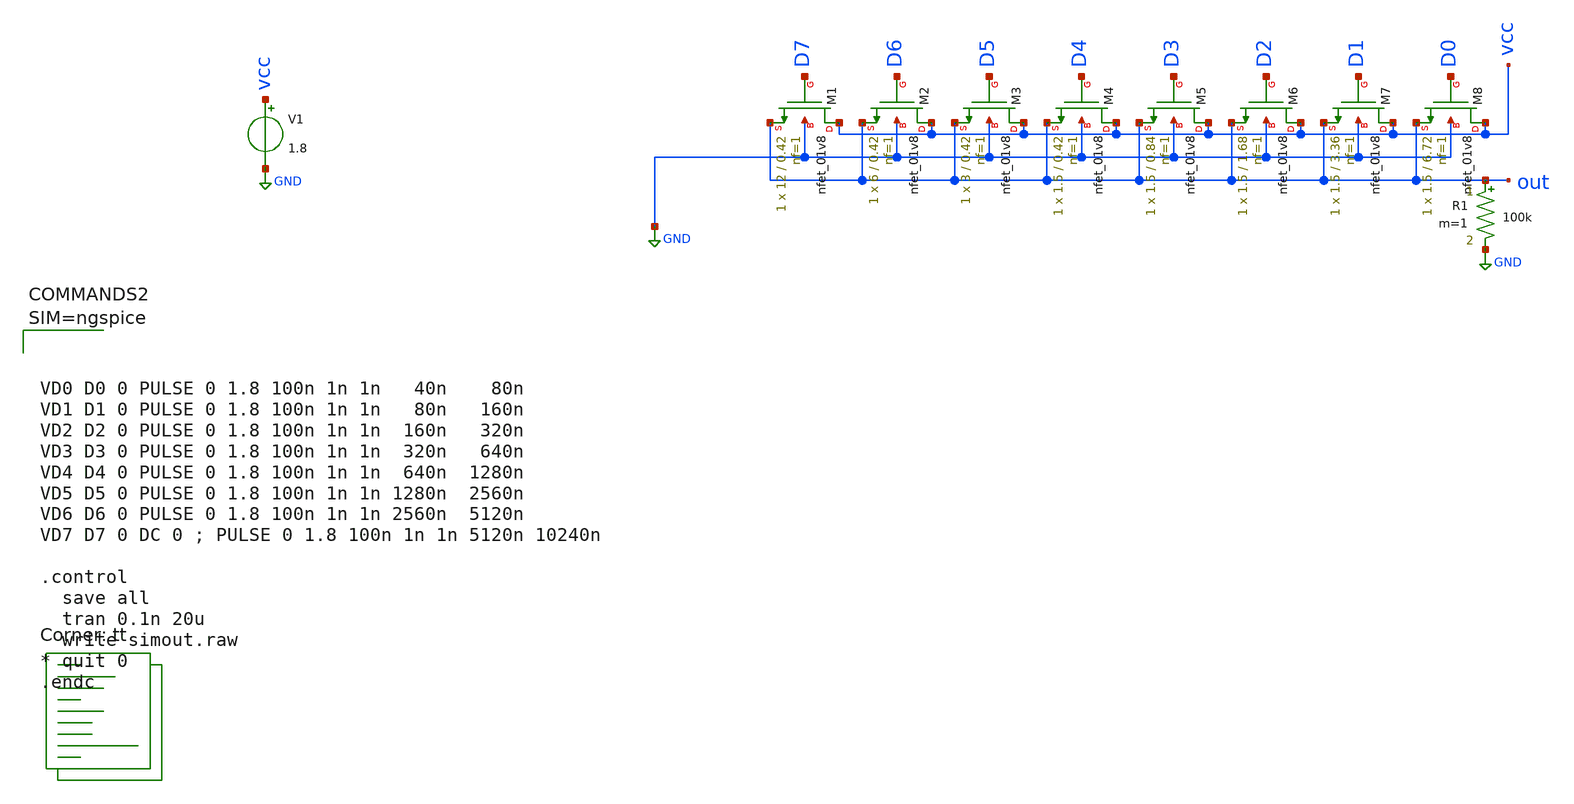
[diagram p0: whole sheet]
** sch_path: xschem/tbtemplate.sch
**.subckt tbtemplate
XM1 vcc D7 out GND sky130_fd_pr__nfet_01v8 L=0.42 W=12 nf=1 ad='int((nf+1)/2) * W/nf * 0.29' as='int((nf+2)/2) * W/nf * 0.29'
+ pd='2*int((nf+1)/2) * (W/nf + 0.29)' ps='2*int((nf+2)/2) * (W/nf + 0.29)' nrd='0.29 / W' nrs='0.29 / W'
+ sa=0 sb=0 sd=0 mult=1 m=1
V1 vcc GND 1.8
XM2 vcc D6 out GND sky130_fd_pr__nfet_01v8 L=0.42 W=6 nf=1 ad='int((nf+1)/2) * W/nf * 0.29' as='int((nf+2)/2) * W/nf * 0.29'
+ pd='2*int((nf+1)/2) * (W/nf + 0.29)' ps='2*int((nf+2)/2) * (W/nf + 0.29)' nrd='0.29 / W' nrs='0.29 / W'
+ sa=0 sb=0 sd=0 mult=1 m=1
XM3 vcc D5 out GND sky130_fd_pr__nfet_01v8 L=0.42 W=3 nf=1 ad='int((nf+1)/2) * W/nf * 0.29' as='int((nf+2)/2) * W/nf * 0.29'
+ pd='2*int((nf+1)/2) * (W/nf + 0.29)' ps='2*int((nf+2)/2) * (W/nf + 0.29)' nrd='0.29 / W' nrs='0.29 / W'
+ sa=0 sb=0 sd=0 mult=1 m=1
XM4 vcc D4 out GND sky130_fd_pr__nfet_01v8 L=0.42 W=1.5 nf=1 ad='int((nf+1)/2) * W/nf * 0.29' as='int((nf+2)/2) * W/nf * 0.29'
+ pd='2*int((nf+1)/2) * (W/nf + 0.29)' ps='2*int((nf+2)/2) * (W/nf + 0.29)' nrd='0.29 / W' nrs='0.29 / W'
+ sa=0 sb=0 sd=0 mult=1 m=1
XM5 vcc D3 out GND sky130_fd_pr__nfet_01v8 L=0.84 W=1.5 nf=1 ad='int((nf+1)/2) * W/nf * 0.29' as='int((nf+2)/2) * W/nf * 0.29'
+ pd='2*int((nf+1)/2) * (W/nf + 0.29)' ps='2*int((nf+2)/2) * (W/nf + 0.29)' nrd='0.29 / W' nrs='0.29 / W'
+ sa=0 sb=0 sd=0 mult=1 m=1
XM6 vcc D2 out GND sky130_fd_pr__nfet_01v8 L=1.68 W=1.5 nf=1 ad='int((nf+1)/2) * W/nf * 0.29' as='int((nf+2)/2) * W/nf * 0.29'
+ pd='2*int((nf+1)/2) * (W/nf + 0.29)' ps='2*int((nf+2)/2) * (W/nf + 0.29)' nrd='0.29 / W' nrs='0.29 / W'
+ sa=0 sb=0 sd=0 mult=1 m=1
XM7 vcc D1 out GND sky130_fd_pr__nfet_01v8 L=3.36 W=1.5 nf=1 ad='int((nf+1)/2) * W/nf * 0.29' as='int((nf+2)/2) * W/nf * 0.29'
+ pd='2*int((nf+1)/2) * (W/nf + 0.29)' ps='2*int((nf+2)/2) * (W/nf + 0.29)' nrd='0.29 / W' nrs='0.29 / W'
+ sa=0 sb=0 sd=0 mult=1 m=1
XM8 vcc D0 out GND sky130_fd_pr__nfet_01v8 L=6.72 W=1.5 nf=1 ad='int((nf+1)/2) * W/nf * 0.29' as='int((nf+2)/2) * W/nf * 0.29'
+ pd='2*int((nf+1)/2) * (W/nf + 0.29)' ps='2*int((nf+2)/2) * (W/nf + 0.29)' nrd='0.29 / W' nrs='0.29 / W'
+ sa=0 sb=0 sd=0 mult=1 m=1
R1 out GND 100k m=1
**** begin user architecture code




VD0 D0 0 PULSE 0 1.8 100n 1n 1n   40n    80n
VD1 D1 0 PULSE 0 1.8 100n 1n 1n   80n   160n
VD2 D2 0 PULSE 0 1.8 100n 1n 1n  160n   320n
VD3 D3 0 PULSE 0 1.8 100n 1n 1n  320n   640n
VD4 D4 0 PULSE 0 1.8 100n 1n 1n  640n  1280n
VD5 D5 0 PULSE 0 1.8 100n 1n 1n 1280n  2560n
VD6 D6 0 PULSE 0 1.8 100n 1n 1n 2560n  5120n
VD7 D7 0 DC 0 ; PULSE 0 1.8 100n 1n 1n 5120n 10240n

.control
  save all
  tran 0.1n 20u
  write simout.raw
* quit 0
.endc




.lib $::SKYWATER_MODELS/sky130.lib.spice tt
**** end user architecture code
**.ends
.GLOBAL GND
.end
